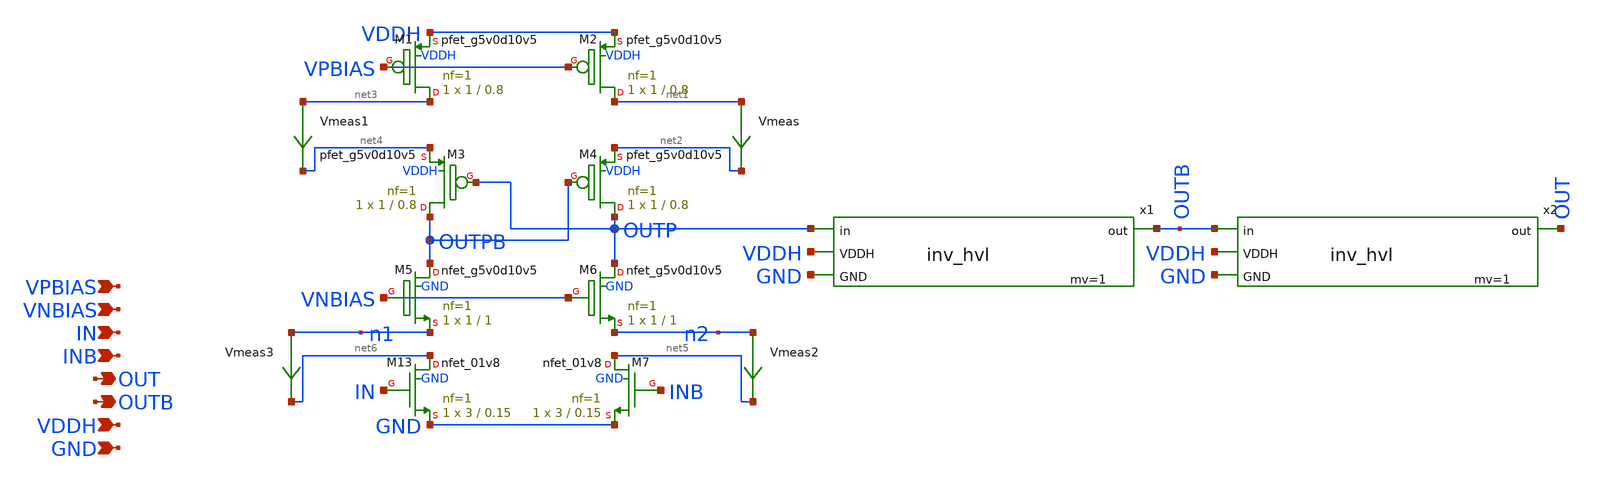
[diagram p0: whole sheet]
** sch_path: xschem/lvsf_1buff.sch
**.subckt lvsf_1buff IN INB OUT VDDH GND VPBIAS VNBIAS OUTB
*.ipin IN
*.ipin INB
*.opin OUT
*.ipin VDDH
*.ipin GND
*.ipin VPBIAS
*.ipin VNBIAS
*.opin OUTB
Vmeas net1 net2 0
.save i(vmeas)
XM13 net6 IN GND GND sky130_fd_pr__nfet_01v8 L=0.15 W=3 nf=1 ad='int((nf+1)/2) * W/nf * 0.29' as='int((nf+2)/2) * W/nf * 0.29'
+ pd='2*int((nf+1)/2) * (W/nf + 0.29)' ps='2*int((nf+2)/2) * (W/nf + 0.29)' nrd='0.29 / W' nrs='0.29 / W'
+ sa=0 sb=0 sd=0 mult=1 m=1
XM1 net3 VPBIAS VDDH VDDH sky130_fd_pr__pfet_g5v0d10v5 L=0.8 W=1 nf=1 ad='int((nf+1)/2) * W/nf * 0.29'
+ as='int((nf+2)/2) * W/nf * 0.29' pd='2*int((nf+1)/2) * (W/nf + 0.29)' ps='2*int((nf+2)/2) * (W/nf + 0.29)'
+ nrd='0.29 / W' nrs='0.29 / W' sa=0 sb=0 sd=0 mult=1 m=1
XM2 net1 VPBIAS VDDH VDDH sky130_fd_pr__pfet_g5v0d10v5 L=0.8 W=1 nf=1 ad='int((nf+1)/2) * W/nf * 0.29'
+ as='int((nf+2)/2) * W/nf * 0.29' pd='2*int((nf+1)/2) * (W/nf + 0.29)' ps='2*int((nf+2)/2) * (W/nf + 0.29)'
+ nrd='0.29 / W' nrs='0.29 / W' sa=0 sb=0 sd=0 mult=1 m=1
XM3 OUTPB OUTP net4 VDDH sky130_fd_pr__pfet_g5v0d10v5 L=0.8 W=1 nf=1 ad='int((nf+1)/2) * W/nf * 0.29'
+ as='int((nf+2)/2) * W/nf * 0.29' pd='2*int((nf+1)/2) * (W/nf + 0.29)' ps='2*int((nf+2)/2) * (W/nf + 0.29)'
+ nrd='0.29 / W' nrs='0.29 / W' sa=0 sb=0 sd=0 mult=1 m=1
XM4 OUTP OUTPB net2 VDDH sky130_fd_pr__pfet_g5v0d10v5 L=0.8 W=1 nf=1 ad='int((nf+1)/2) * W/nf * 0.29'
+ as='int((nf+2)/2) * W/nf * 0.29' pd='2*int((nf+1)/2) * (W/nf + 0.29)' ps='2*int((nf+2)/2) * (W/nf + 0.29)'
+ nrd='0.29 / W' nrs='0.29 / W' sa=0 sb=0 sd=0 mult=1 m=1
XM5 OUTPB VNBIAS n1 GND sky130_fd_pr__nfet_g5v0d10v5 L=1 W=1 nf=1 ad='int((nf+1)/2) * W/nf * 0.29' as='int((nf+2)/2) * W/nf * 0.29'
+ pd='2*int((nf+1)/2) * (W/nf + 0.29)' ps='2*int((nf+2)/2) * (W/nf + 0.29)' nrd='0.29 / W' nrs='0.29 / W'
+ sa=0 sb=0 sd=0 mult=1 m=1
XM6 OUTP VNBIAS n2 GND sky130_fd_pr__nfet_g5v0d10v5 L=1 W=1 nf=1 ad='int((nf+1)/2) * W/nf * 0.29' as='int((nf+2)/2) * W/nf * 0.29'
+ pd='2*int((nf+1)/2) * (W/nf + 0.29)' ps='2*int((nf+2)/2) * (W/nf + 0.29)' nrd='0.29 / W' nrs='0.29 / W'
+ sa=0 sb=0 sd=0 mult=1 m=1
Vmeas1 net3 net4 0
.save i(vmeas1)
XM7 net5 INB GND GND sky130_fd_pr__nfet_01v8 L=0.15 W=3 nf=1 ad='int((nf+1)/2) * W/nf * 0.29' as='int((nf+2)/2) * W/nf * 0.29'
+ pd='2*int((nf+1)/2) * (W/nf + 0.29)' ps='2*int((nf+2)/2) * (W/nf + 0.29)' nrd='0.29 / W' nrs='0.29 / W'
+ sa=0 sb=0 sd=0 mult=1 m=1
Vmeas2 n2 net5 0
.save i(vmeas2)
Vmeas3 n1 net6 0
.save i(vmeas3)
x1 OUTP OUTB VDDH GND inv_hvl mv=1
x2 OUTB OUT VDDH GND inv_hvl mv=1
**.ends

* expanding   symbol:  inv_hvl.sym # of pins=4
** sym_path: xschem/inv_hvl.sym
** sch_path: xschem/inv_hvl.sch
.subckt inv_hvl in out VDDH GND  mv=1
*.opin out
*.ipin VDDH
*.ipin GND
*.ipin in
.param wp=0.84 wn=0.42 l=0.5
XM1 out in VDDH VDDH sky130_fd_pr__pfet_g5v0d10v5 L=l W=wp nf=1 ad='int((nf+1)/2) * W/nf * 0.29' as='int((nf+2)/2) * W/nf * 0.29'
+ pd='2*int((nf+1)/2) * (W/nf + 0.29)' ps='2*int((nf+2)/2) * (W/nf + 0.29)' nrd='0.29 / W' nrs='0.29 / W'
+ sa=0 sb=0 sd=0 mult=mv m=mv
XM2 out in GND GND sky130_fd_pr__nfet_g5v0d10v5 L=l W=wn nf=1 ad='int((nf+1)/2) * W/nf * 0.29' as='int((nf+2)/2) * W/nf * 0.29'
+ pd='2*int((nf+1)/2) * (W/nf + 0.29)' ps='2*int((nf+2)/2) * (W/nf + 0.29)' nrd='0.29 / W' nrs='0.29 / W'
+ sa=0 sb=0 sd=0 mult=mv m=mv
.ends

.end
